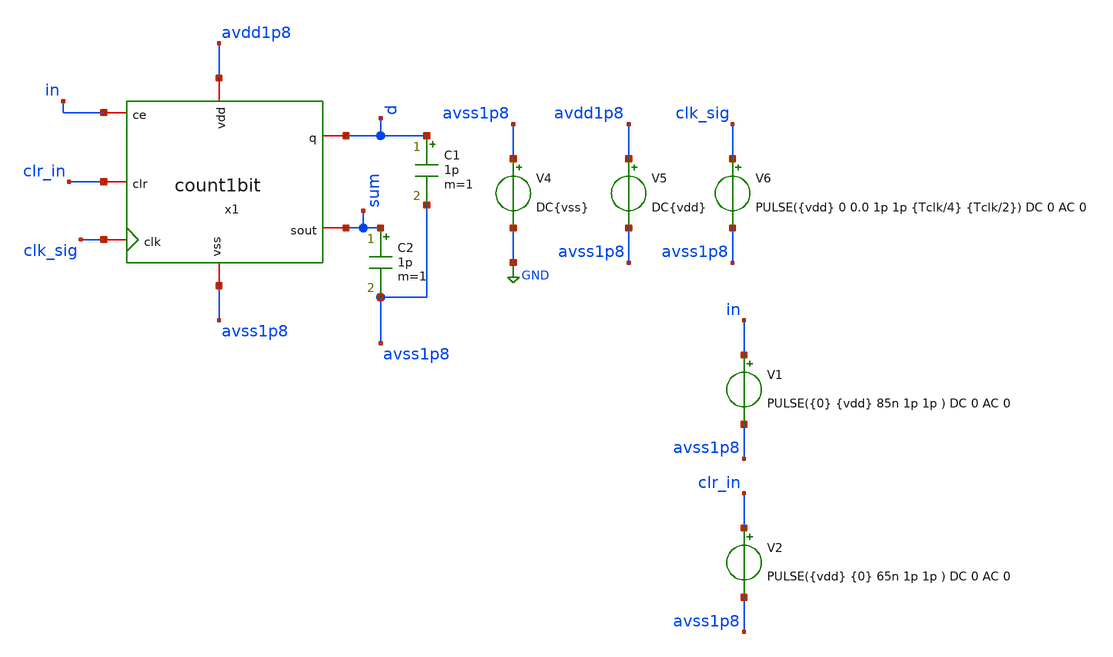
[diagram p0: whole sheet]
** sch_path: verification/testbenches/tb2_count1bit.sch
**.subckt tb2_count1bit
V4 avss1p8 GND DC{vss}
V5 avdd1p8 avss1p8 DC{vdd}
V6 clk_sig avss1p8 PULSE({vdd} 0 0.0 1p 1p {Tclk/4} {Tclk/2}) DC 0 AC 0
x1 avdd1p8 avss1p8 in d clr_in clk_sig sum count1bit
C1 d avss1p8 1p m=1
C2 sum avss1p8 1p m=1
V1 in avss1p8 PULSE({0} {vdd} 85n 1p 1p ) DC 0 AC 0
V2 clr_in avss1p8 PULSE({vdd} {0} 65n 1p 1p ) DC 0 AC 0
**** begin user architecture code


* Circuit Parameters
.param vdd = 1.2
.param vss = 0.0
.param Tclk = 100n
.param Tin = 1000n
.options TEMP = 27.0
* Include Models - IHP SG13G2
.lib cornerMOSlv.lib mos_tt
* OP Parameters & Singals to save
.save all
*Simulations
.control
tran 0.1u 1000n
setplot tran1
plot v(clk_sig) v(sum)+1.2 v(d)+2.4 v(in)+3.6
reset
dc V6 0 1.2 0.01
setplot dc
set filetype = ascii
write dcsweep.raw
.endc
.end


**** end user architecture code
**.ends
.GLOBAL GND
.end
